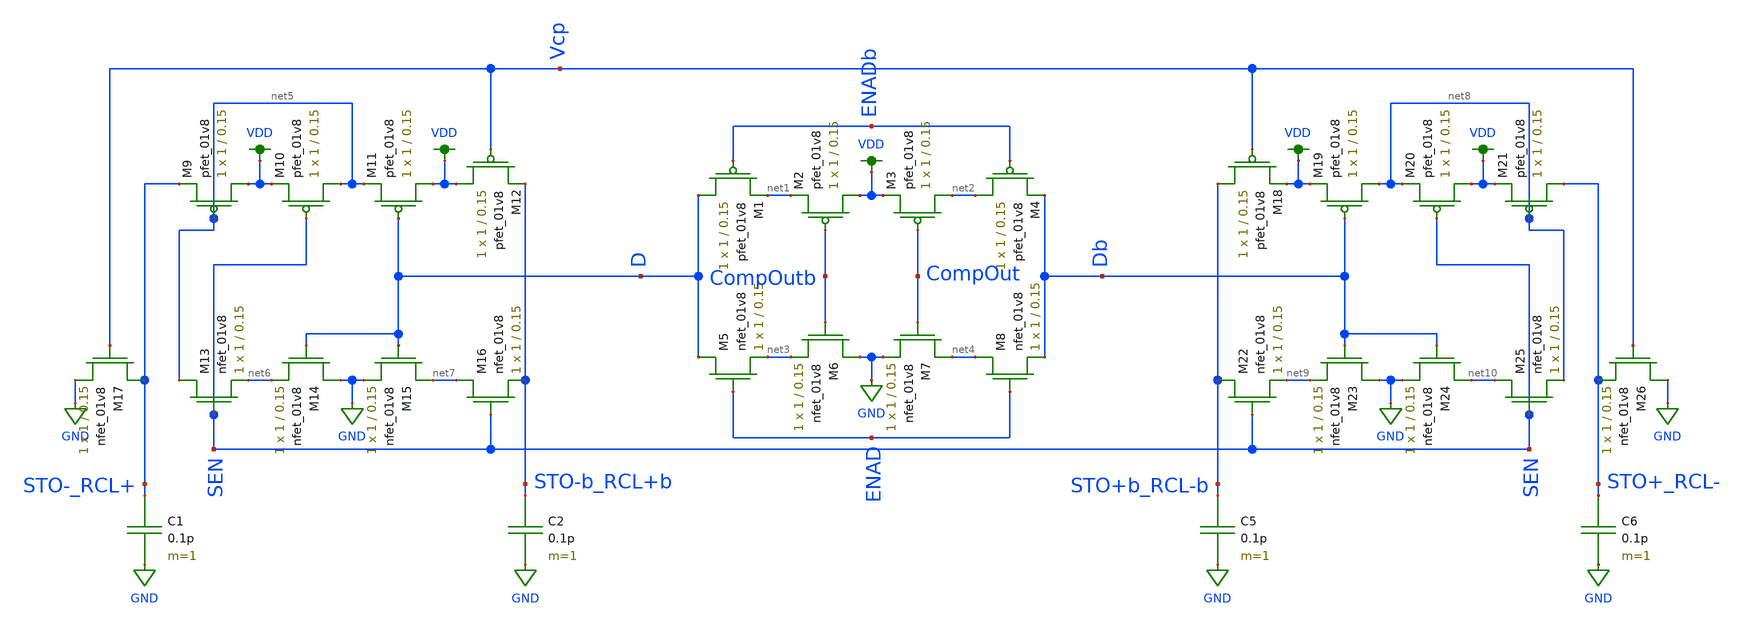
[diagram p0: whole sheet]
** sch_path: schematics/LDS/digital_lds.sch
**.subckt digital_lds
XM1 D ENADb net1 VDD sky130_fd_pr__pfet_01v8 L=0.15 W=1 nf=1 ad='int((nf+1)/2) * W/nf * 0.29' as='int((nf+2)/2) * W/nf * 0.29'
+ pd='2*int((nf+1)/2) * (W/nf + 0.29)' ps='2*int((nf+2)/2) * (W/nf + 0.29)' nrd='0.29 / W' nrs='0.29 / W'
+ sa=0 sb=0 sd=0 mult=1 m=1
XM2 VDD CompOutb net1 VDD sky130_fd_pr__pfet_01v8 L=0.15 W=1 nf=1 ad='int((nf+1)/2) * W/nf * 0.29' as='int((nf+2)/2) * W/nf * 0.29'
+ pd='2*int((nf+1)/2) * (W/nf + 0.29)' ps='2*int((nf+2)/2) * (W/nf + 0.29)' nrd='0.29 / W' nrs='0.29 / W'
+ sa=0 sb=0 sd=0 mult=1 m=1
XM3 net2 CompOut VDD VDD sky130_fd_pr__pfet_01v8 L=0.15 W=1 nf=1 ad='int((nf+1)/2) * W/nf * 0.29' as='int((nf+2)/2) * W/nf * 0.29'
+ pd='2*int((nf+1)/2) * (W/nf + 0.29)' ps='2*int((nf+2)/2) * (W/nf + 0.29)' nrd='0.29 / W' nrs='0.29 / W'
+ sa=0 sb=0 sd=0 mult=1 m=1
XM4 net2 ENADb Db VDD sky130_fd_pr__pfet_01v8 L=0.15 W=1 nf=1 ad='int((nf+1)/2) * W/nf * 0.29' as='int((nf+2)/2) * W/nf * 0.29'
+ pd='2*int((nf+1)/2) * (W/nf + 0.29)' ps='2*int((nf+2)/2) * (W/nf + 0.29)' nrd='0.29 / W' nrs='0.29 / W'
+ sa=0 sb=0 sd=0 mult=1 m=1
XM5 D ENAD net3 GND sky130_fd_pr__nfet_01v8 L=0.15 W=1 nf=1 ad='int((nf+1)/2) * W/nf * 0.29' as='int((nf+2)/2) * W/nf * 0.29'
+ pd='2*int((nf+1)/2) * (W/nf + 0.29)' ps='2*int((nf+2)/2) * (W/nf + 0.29)' nrd='0.29 / W' nrs='0.29 / W'
+ sa=0 sb=0 sd=0 mult=1 m=1
XM6 GND CompOutb net3 GND sky130_fd_pr__nfet_01v8 L=0.15 W=1 nf=1 ad='int((nf+1)/2) * W/nf * 0.29' as='int((nf+2)/2) * W/nf * 0.29'
+ pd='2*int((nf+1)/2) * (W/nf + 0.29)' ps='2*int((nf+2)/2) * (W/nf + 0.29)' nrd='0.29 / W' nrs='0.29 / W'
+ sa=0 sb=0 sd=0 mult=1 m=1
XM7 net4 CompOut GND GND sky130_fd_pr__nfet_01v8 L=0.15 W=1 nf=1 ad='int((nf+1)/2) * W/nf * 0.29' as='int((nf+2)/2) * W/nf * 0.29'
+ pd='2*int((nf+1)/2) * (W/nf + 0.29)' ps='2*int((nf+2)/2) * (W/nf + 0.29)' nrd='0.29 / W' nrs='0.29 / W'
+ sa=0 sb=0 sd=0 mult=1 m=1
XM8 net4 ENAD Db GND sky130_fd_pr__nfet_01v8 L=0.15 W=1 nf=1 ad='int((nf+1)/2) * W/nf * 0.29' as='int((nf+2)/2) * W/nf * 0.29'
+ pd='2*int((nf+1)/2) * (W/nf + 0.29)' ps='2*int((nf+2)/2) * (W/nf + 0.29)' nrd='0.29 / W' nrs='0.29 / W'
+ sa=0 sb=0 sd=0 mult=1 m=1
XM9 VDD net5 STO-_RCL+ VDD sky130_fd_pr__pfet_01v8 L=0.15 W=1 nf=1 ad='int((nf+1)/2) * W/nf * 0.29' as='int((nf+2)/2) * W/nf * 0.29'
+ pd='2*int((nf+1)/2) * (W/nf + 0.29)' ps='2*int((nf+2)/2) * (W/nf + 0.29)' nrd='0.29 / W' nrs='0.29 / W'
+ sa=0 sb=0 sd=0 mult=1 m=1
XM10 net5 SEN VDD VDD sky130_fd_pr__pfet_01v8 L=0.15 W=1 nf=1 ad='int((nf+1)/2) * W/nf * 0.29' as='int((nf+2)/2) * W/nf * 0.29'
+ pd='2*int((nf+1)/2) * (W/nf + 0.29)' ps='2*int((nf+2)/2) * (W/nf + 0.29)' nrd='0.29 / W' nrs='0.29 / W'
+ sa=0 sb=0 sd=0 mult=1 m=1
XM11 VDD D net5 VDD sky130_fd_pr__pfet_01v8 L=0.15 W=1 nf=1 ad='int((nf+1)/2) * W/nf * 0.29' as='int((nf+2)/2) * W/nf * 0.29'
+ pd='2*int((nf+1)/2) * (W/nf + 0.29)' ps='2*int((nf+2)/2) * (W/nf + 0.29)' nrd='0.29 / W' nrs='0.29 / W'
+ sa=0 sb=0 sd=0 mult=1 m=1
XM12 VDD Vcp STO-b_RCL+b VDD sky130_fd_pr__pfet_01v8 L=0.15 W=1 nf=1 ad='int((nf+1)/2) * W/nf * 0.29'
+ as='int((nf+2)/2) * W/nf * 0.29' pd='2*int((nf+1)/2) * (W/nf + 0.29)' ps='2*int((nf+2)/2) * (W/nf + 0.29)'
+ nrd='0.29 / W' nrs='0.29 / W' sa=0 sb=0 sd=0 mult=1 m=1
XM13 net5 SEN net6 GND sky130_fd_pr__nfet_01v8 L=0.15 W=1 nf=1 ad='int((nf+1)/2) * W/nf * 0.29' as='int((nf+2)/2) * W/nf * 0.29'
+ pd='2*int((nf+1)/2) * (W/nf + 0.29)' ps='2*int((nf+2)/2) * (W/nf + 0.29)' nrd='0.29 / W' nrs='0.29 / W'
+ sa=0 sb=0 sd=0 mult=1 m=1
XM14 GND D net6 GND sky130_fd_pr__nfet_01v8 L=0.15 W=1 nf=1 ad='int((nf+1)/2) * W/nf * 0.29' as='int((nf+2)/2) * W/nf * 0.29'
+ pd='2*int((nf+1)/2) * (W/nf + 0.29)' ps='2*int((nf+2)/2) * (W/nf + 0.29)' nrd='0.29 / W' nrs='0.29 / W'
+ sa=0 sb=0 sd=0 mult=1 m=1
XM15 net7 D GND GND sky130_fd_pr__nfet_01v8 L=0.15 W=1 nf=1 ad='int((nf+1)/2) * W/nf * 0.29' as='int((nf+2)/2) * W/nf * 0.29'
+ pd='2*int((nf+1)/2) * (W/nf + 0.29)' ps='2*int((nf+2)/2) * (W/nf + 0.29)' nrd='0.29 / W' nrs='0.29 / W'
+ sa=0 sb=0 sd=0 mult=1 m=1
XM16 net7 SEN STO-b_RCL+b GND sky130_fd_pr__nfet_01v8 L=0.15 W=1 nf=1 ad='int((nf+1)/2) * W/nf * 0.29'
+ as='int((nf+2)/2) * W/nf * 0.29' pd='2*int((nf+1)/2) * (W/nf + 0.29)' ps='2*int((nf+2)/2) * (W/nf + 0.29)'
+ nrd='0.29 / W' nrs='0.29 / W' sa=0 sb=0 sd=0 mult=1 m=1
XM17 STO-_RCL+ Vcp GND GND sky130_fd_pr__nfet_01v8 L=0.15 W=1 nf=1 ad='int((nf+1)/2) * W/nf * 0.29' as='int((nf+2)/2) * W/nf * 0.29'
+ pd='2*int((nf+1)/2) * (W/nf + 0.29)' ps='2*int((nf+2)/2) * (W/nf + 0.29)' nrd='0.29 / W' nrs='0.29 / W'
+ sa=0 sb=0 sd=0 mult=1 m=1
C1 STO-_RCL+ GND 0.1p m=1
C2 STO-b_RCL+b GND 0.1p m=1
XM18 STO+b_RCL-b Vcp VDD VDD sky130_fd_pr__pfet_01v8 L=0.15 W=1 nf=1 ad='int((nf+1)/2) * W/nf * 0.29'
+ as='int((nf+2)/2) * W/nf * 0.29' pd='2*int((nf+1)/2) * (W/nf + 0.29)' ps='2*int((nf+2)/2) * (W/nf + 0.29)'
+ nrd='0.29 / W' nrs='0.29 / W' sa=0 sb=0 sd=0 mult=1 m=1
XM19 net8 Db VDD VDD sky130_fd_pr__pfet_01v8 L=0.15 W=1 nf=1 ad='int((nf+1)/2) * W/nf * 0.29' as='int((nf+2)/2) * W/nf * 0.29'
+ pd='2*int((nf+1)/2) * (W/nf + 0.29)' ps='2*int((nf+2)/2) * (W/nf + 0.29)' nrd='0.29 / W' nrs='0.29 / W'
+ sa=0 sb=0 sd=0 mult=1 m=1
XM20 VDD SEN net8 VDD sky130_fd_pr__pfet_01v8 L=0.15 W=1 nf=1 ad='int((nf+1)/2) * W/nf * 0.29' as='int((nf+2)/2) * W/nf * 0.29'
+ pd='2*int((nf+1)/2) * (W/nf + 0.29)' ps='2*int((nf+2)/2) * (W/nf + 0.29)' nrd='0.29 / W' nrs='0.29 / W'
+ sa=0 sb=0 sd=0 mult=1 m=1
XM21 STO+_RCL- net8 VDD VDD sky130_fd_pr__pfet_01v8 L=0.15 W=1 nf=1 ad='int((nf+1)/2) * W/nf * 0.29'
+ as='int((nf+2)/2) * W/nf * 0.29' pd='2*int((nf+1)/2) * (W/nf + 0.29)' ps='2*int((nf+2)/2) * (W/nf + 0.29)'
+ nrd='0.29 / W' nrs='0.29 / W' sa=0 sb=0 sd=0 mult=1 m=1
XM22 STO+b_RCL-b SEN net9 GND sky130_fd_pr__nfet_01v8 L=0.15 W=1 nf=1 ad='int((nf+1)/2) * W/nf * 0.29'
+ as='int((nf+2)/2) * W/nf * 0.29' pd='2*int((nf+1)/2) * (W/nf + 0.29)' ps='2*int((nf+2)/2) * (W/nf + 0.29)'
+ nrd='0.29 / W' nrs='0.29 / W' sa=0 sb=0 sd=0 mult=1 m=1
XM23 GND Db net9 GND sky130_fd_pr__nfet_01v8 L=0.15 W=1 nf=1 ad='int((nf+1)/2) * W/nf * 0.29' as='int((nf+2)/2) * W/nf * 0.29'
+ pd='2*int((nf+1)/2) * (W/nf + 0.29)' ps='2*int((nf+2)/2) * (W/nf + 0.29)' nrd='0.29 / W' nrs='0.29 / W'
+ sa=0 sb=0 sd=0 mult=1 m=1
XM24 net10 Db GND GND sky130_fd_pr__nfet_01v8 L=0.15 W=1 nf=1 ad='int((nf+1)/2) * W/nf * 0.29' as='int((nf+2)/2) * W/nf * 0.29'
+ pd='2*int((nf+1)/2) * (W/nf + 0.29)' ps='2*int((nf+2)/2) * (W/nf + 0.29)' nrd='0.29 / W' nrs='0.29 / W'
+ sa=0 sb=0 sd=0 mult=1 m=1
XM25 net10 SEN net8 GND sky130_fd_pr__nfet_01v8 L=0.15 W=1 nf=1 ad='int((nf+1)/2) * W/nf * 0.29' as='int((nf+2)/2) * W/nf * 0.29'
+ pd='2*int((nf+1)/2) * (W/nf + 0.29)' ps='2*int((nf+2)/2) * (W/nf + 0.29)' nrd='0.29 / W' nrs='0.29 / W'
+ sa=0 sb=0 sd=0 mult=1 m=1
XM26 GND Vcp STO+_RCL- GND sky130_fd_pr__nfet_01v8 L=0.15 W=1 nf=1 ad='int((nf+1)/2) * W/nf * 0.29' as='int((nf+2)/2) * W/nf * 0.29'
+ pd='2*int((nf+1)/2) * (W/nf + 0.29)' ps='2*int((nf+2)/2) * (W/nf + 0.29)' nrd='0.29 / W' nrs='0.29 / W'
+ sa=0 sb=0 sd=0 mult=1 m=1
C5 STO+b_RCL-b GND 0.1p m=1
C6 STO+_RCL- GND 0.1p m=1
**.ends
.GLOBAL VDD
.GLOBAL GND
.end
